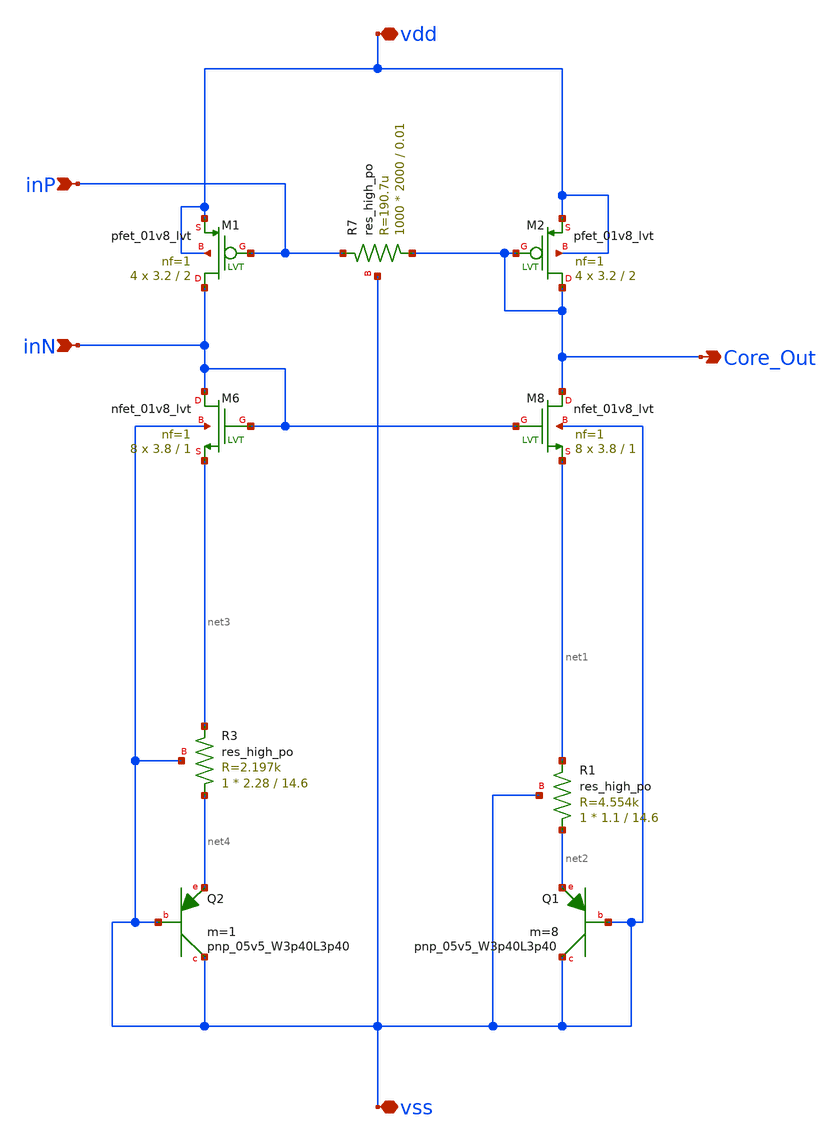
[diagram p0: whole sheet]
** sch_path: BGR_core.sch
**.subckt BGR_core vdd vss inP inN Core_Out
*.iopin vdd
*.iopin vss
*.ipin inP
*.ipin inN
*.opin Core_Out
XM6 inN inN net3 vss sky130_fd_pr__nfet_01v8_lvt L=1 W=3.8 nf=1 ad='int((1 + 1)/2) * 3.8 / 1 * 0.29'
+ as='int((1 + 2)/2) * 3.8 / 1 * 0.29' pd='2*int((1 + 1)/2) * (3.8 / 1 + 0.29)' ps='2*int((1 + 2)/2) * (3.8 / 1 + 0.29)'
+ nrd='0.29 / 3.8 ' nrs='0.29 / 3.8 ' sa=0 sb=0 sd=0 mult=8 m=8
XM1 inN inP vdd vdd sky130_fd_pr__pfet_01v8_lvt L=2 W=3.2 nf=1 ad='int((1 + 1)/2) * 3.2 / 1 * 0.29' as='int((1 + 2)/2) * 3.2 / 1 * 0.29'
+ pd='2*int((1 + 1)/2) * (3.2 / 1 + 0.29)' ps='2*int((1 + 2)/2) * (3.2 / 1 + 0.29)' nrd='0.29 / 3.2 ' nrs='0.29 / 3.2 '
+ sa=0 sb=0 sd=0 mult=4 m=4
XQ1 vss vss net2 sky130_fd_pr__pnp_05v5_W3p40L3p40 m=8
XR1 net2 net1 vss sky130_fd_pr__res_high_po W=1.1 L=14.6 mult=1 m=1
XM2 Core_Out Core_Out vdd vdd sky130_fd_pr__pfet_01v8_lvt L=2 W=3.2 nf=1 ad='int((1 + 1)/2) * 3.2 / 1 * 0.29'
+ as='int((1 + 2)/2) * 3.2 / 1 * 0.29' pd='2*int((1 + 1)/2) * (3.2 / 1 + 0.29)' ps='2*int((1 + 2)/2) * (3.2 / 1 + 0.29)'
+ nrd='0.29 / 3.2 ' nrs='0.29 / 3.2 ' sa=0 sb=0 sd=0 mult=4 m=4
XM8 Core_Out inN net1 vss sky130_fd_pr__nfet_01v8_lvt L=1 W=3.8 nf=1 ad='int((1 + 1)/2) * 3.8 / 1 * 0.29'
+ as='int((1 + 2)/2) * 3.8 / 1 * 0.29' pd='2*int((1 + 1)/2) * (3.8 / 1 + 0.29)' ps='2*int((1 + 2)/2) * (3.8 / 1 + 0.29)'
+ nrd='0.29 / 3.8 ' nrs='0.29 / 3.8 ' sa=0 sb=0 sd=0 mult=8 m=8
XQ2 vss vss net4 sky130_fd_pr__pnp_05v5_W3p40L3p40 m=1
XR3 net4 net3 vss sky130_fd_pr__res_high_po W=2.28 L=14.6 mult=1 m=1
XR7 Core_Out inP vss sky130_fd_pr__res_high_po W=2000 L=0.01 mult=1000 m=1000
**.ends
.end
